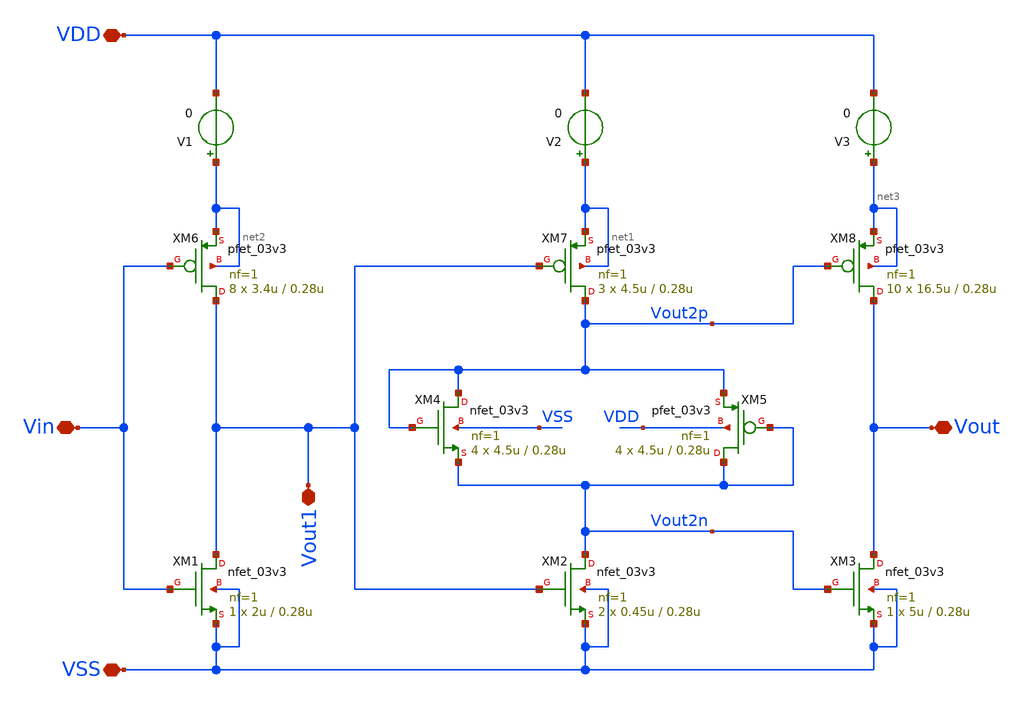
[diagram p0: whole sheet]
** sch_path: designs/DS_modulator/ring_amp/xschem/ring_amp.sch
**.subckt ring_amp VDD VSS Vin Vout Vout1
*.iopin VDD
*.iopin VSS
*.iopin Vin
*.iopin Vout
*.iopin Vout1
XM1 Vout1 Vin VSS VSS nfet_03v3 L=0.28u W=2u nf=1 ad='int((nf+1)/2) * W/nf * 0.18u' as='int((nf+2)/2) * W/nf * 0.18u'
+ pd='2*int((nf+1)/2) * (W/nf + 0.18u)' ps='2*int((nf+2)/2) * (W/nf + 0.18u)' nrd='0.18u / W' nrs='0.18u / W'
+ sa=0 sb=0 sd=0 m=1
XM4 Vout2p Vout2p Vout2n VSS nfet_03v3 L=0.28u W=4.5u nf=1 ad='int((nf+1)/2) * W/nf * 0.18u' as='int((nf+2)/2) * W/nf * 0.18u'
+ pd='2*int((nf+1)/2) * (W/nf + 0.18u)' ps='2*int((nf+2)/2) * (W/nf + 0.18u)' nrd='0.18u / W' nrs='0.18u / W'
+ sa=0 sb=0 sd=0 m=4
XM3 Vout Vout2n VSS VSS nfet_03v3 L=0.28u W=5u nf=1 ad='int((nf+1)/2) * W/nf * 0.18u' as='int((nf+2)/2) * W/nf * 0.18u'
+ pd='2*int((nf+1)/2) * (W/nf + 0.18u)' ps='2*int((nf+2)/2) * (W/nf + 0.18u)' nrd='0.18u / W' nrs='0.18u / W'
+ sa=0 sb=0 sd=0 m=1
XM5 Vout2n Vout2n Vout2p VDD pfet_03v3 L=0.28u W=4.5u nf=1 ad='int((nf+1)/2) * W/nf * 0.18u' as='int((nf+2)/2) * W/nf * 0.18u'
+ pd='2*int((nf+1)/2) * (W/nf + 0.18u)' ps='2*int((nf+2)/2) * (W/nf + 0.18u)' nrd='0.18u / W' nrs='0.18u / W'
+ sa=0 sb=0 sd=0 m=4
XM6 Vout1 Vin net2 net2 pfet_03v3 L=0.28u W=3.4u nf=1 ad='int((nf+1)/2) * W/nf * 0.18u' as='int((nf+2)/2) * W/nf * 0.18u'
+ pd='2*int((nf+1)/2) * (W/nf + 0.18u)' ps='2*int((nf+2)/2) * (W/nf + 0.18u)' nrd='0.18u / W' nrs='0.18u / W'
+ sa=0 sb=0 sd=0 m=8
XM8 Vout Vout2p net3 net3 pfet_03v3 L=0.28u W=16.5u nf=1 ad='int((nf+1)/2) * W/nf * 0.18u' as='int((nf+2)/2) * W/nf * 0.18u'
+ pd='2*int((nf+1)/2) * (W/nf + 0.18u)' ps='2*int((nf+2)/2) * (W/nf + 0.18u)' nrd='0.18u / W' nrs='0.18u / W'
+ sa=0 sb=0 sd=0 m=10
V1 net2 VDD 0
.save i(v1)
V2 net1 VDD 0
.save i(v2)
V3 net3 VDD 0
.save i(v3)
XM2 Vout2n Vout1 VSS VSS nfet_03v3 L=0.28u W=0.45u nf=1 ad='int((nf+1)/2) * W/nf * 0.18u' as='int((nf+2)/2) * W/nf * 0.18u'
+ pd='2*int((nf+1)/2) * (W/nf + 0.18u)' ps='2*int((nf+2)/2) * (W/nf + 0.18u)' nrd='0.18u / W' nrs='0.18u / W'
+ sa=0 sb=0 sd=0 m=2
XM7 Vout2p Vout1 net1 net1 pfet_03v3 L=0.28u W=4.5u nf=1 ad='int((nf+1)/2) * W/nf * 0.18u' as='int((nf+2)/2) * W/nf * 0.18u'
+ pd='2*int((nf+1)/2) * (W/nf + 0.18u)' ps='2*int((nf+2)/2) * (W/nf + 0.18u)' nrd='0.18u / W' nrs='0.18u / W'
+ sa=0 sb=0 sd=0 m=3
**.ends
.end
